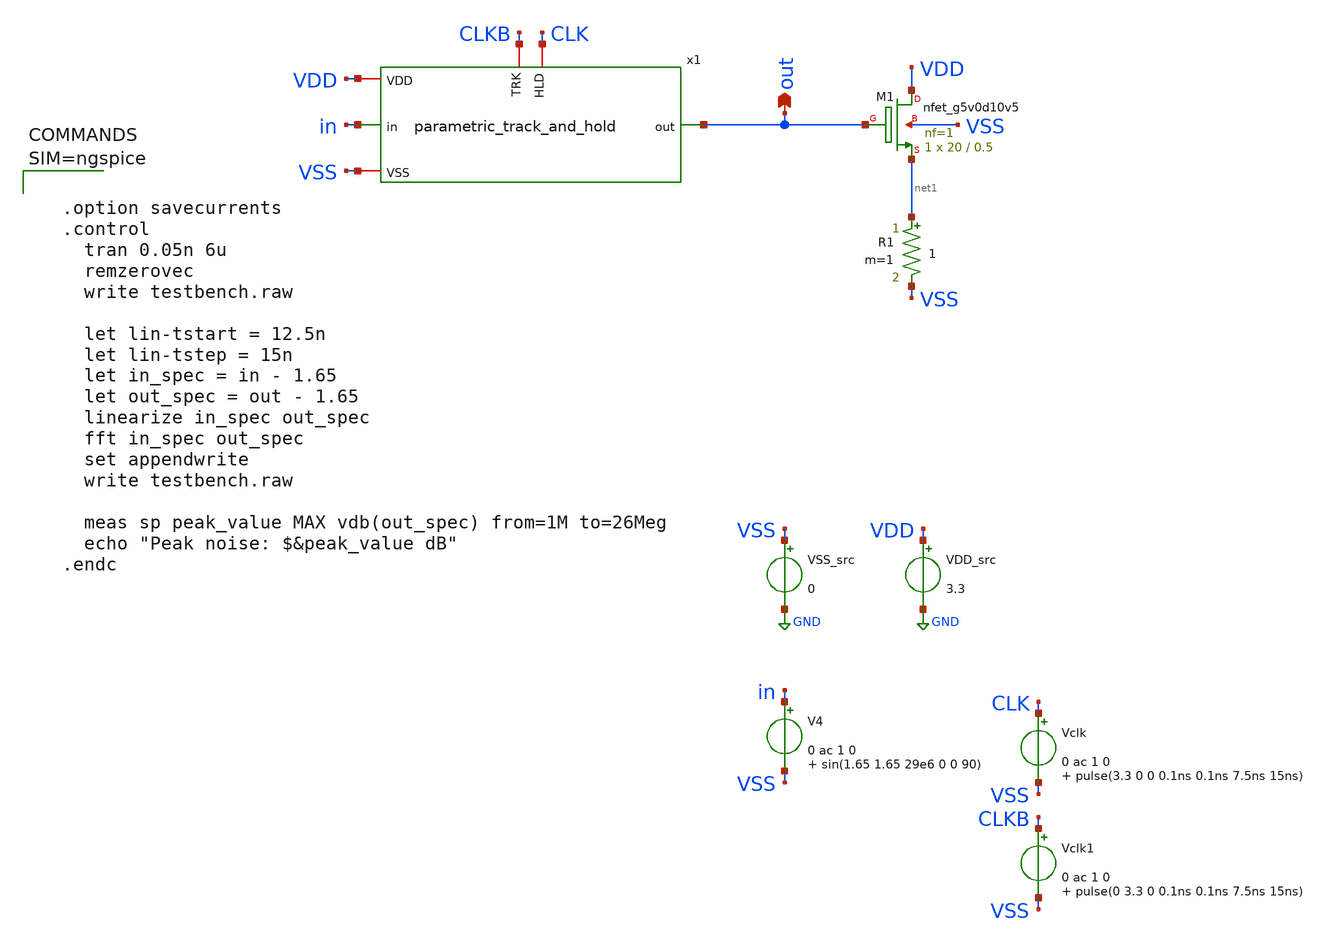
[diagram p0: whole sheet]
** sch_path: xschem/testbench.sch
**.subckt testbench out
*.opin out
VDD_src VDD GND 3.3
VSS_src VSS GND 0
V4 in VSS 0 ac 1 0 sin(1.65 1.65 29e6 0 0 90)
XM1 VDD out net1 VSS sky130_fd_pr__nfet_g5v0d10v5 L=0.5 W=20 nf=1 ad='int((nf+1)/2) * W/nf * 0.29' as='int((nf+2)/2) * W/nf * 0.29'
+ pd='2*int((nf+1)/2) * (W/nf + 0.29)' ps='2*int((nf+2)/2) * (W/nf + 0.29)' nrd='0.29 / W' nrs='0.29 / W'
+ sa=0 sb=0 sd=0 mult=1 m=1
R1 net1 VSS 1 m=1
Vclk CLK VSS 0 ac 1 0 pulse(3.3 0 0 0.1ns 0.1ns 7.5ns 15ns)
Vclk1 CLKB VSS 0 ac 1 0 pulse(0 3.3 0 0.1ns 0.1ns 7.5ns 15ns)
x1 CLK CLKB VDD VSS out in parametric_track_and_hold WT=1 PFT=1.21 PF=2 WS=5 WB=5 CB=18
**** begin user architecture code

** opencircuitdesign pdks install
.lib $::SKYWATER_MODELS/sky130.lib.spice tt





  .option savecurrents
  .control
    tran 0.05n 6u
    remzerovec
    write testbench.raw

    let lin-tstart = 12.5n
    let lin-tstep = 15n
    let in_spec = in - 1.65
    let out_spec = out - 1.65
    linearize in_spec out_spec
    fft in_spec out_spec
    set appendwrite
    write testbench.raw

    meas sp peak_value MAX vdb(out_spec) from=1M to=26Meg
    echo "Peak noise: $&peak_value dB"
  .endc



**** end user architecture code
**.ends

* expanding   symbol:  parametric_track_and_hold.sym # of pins=6
** sym_path: xschem/parametric_track_and_hold.sym
** sch_path: xschem/parametric_track_and_hold.sch
.subckt parametric_track_and_hold HLD TRK VDD VSS out in  WT=1 PFT=1.21 PF=2 WS=5 WB=5 CB=18
*.iopin VSS
*.iopin VDD
*.ipin in
*.opin out
*.iopin TRK
*.iopin HLD
XC1 out VSS sky130_fd_pr__cap_mim_m3_1 W=5 L=5 MF=1 m=1
XM1 out X in VSS sky130_fd_pr__nfet_g5v0d10v5 L=0.5 W={WT} nf=1 ad='int((nf+1)/2) * W/nf * 0.29' as='int((nf+2)/2) * W/nf * 0.29'
+ pd='2*int((nf+1)/2) * (W/nf + 0.29)' ps='2*int((nf+2)/2) * (W/nf + 0.29)' nrd='0.29 / W' nrs='0.29 / W'
+ sa=0 sb=0 sd=0 mult=1 m=1
XM1p out net1 in VDD sky130_fd_pr__pfet_g5v0d10v5 L=0.5 W={WT*PFT} nf=1 ad='int((nf+1)/2) * W/nf * 0.29'
+ as='int((nf+2)/2) * W/nf * 0.29' pd='2*int((nf+1)/2) * (W/nf + 0.29)' ps='2*int((nf+2)/2) * (W/nf + 0.29)'
+ nrd='0.29 / W' nrs='0.29 / W' sa=0 sb=0 sd=0 mult=1 m=1
XM4 VSS HLD X VSS sky130_fd_pr__nfet_g5v0d10v5 L=0.5 W={WS} nf=1 ad='int((nf+1)/2) * W/nf * 0.29' as='int((nf+2)/2) * W/nf * 0.29'
+ pd='2*int((nf+1)/2) * (W/nf + 0.29)' ps='2*int((nf+2)/2) * (W/nf + 0.29)' nrd='0.29 / W' nrs='0.29 / W'
+ sa=0 sb=0 sd=0 mult=1 m=1
XM4p net1 TRK VDD VDD sky130_fd_pr__pfet_g5v0d10v5 L=0.5 W={WS*PF} nf=1 ad='int((nf+1)/2) * W/nf * 0.29'
+ as='int((nf+2)/2) * W/nf * 0.29' pd='2*int((nf+1)/2) * (W/nf + 0.29)' ps='2*int((nf+2)/2) * (W/nf + 0.29)'
+ nrd='0.29 / W' nrs='0.29 / W' sa=0 sb=0 sd=0 mult=1 m=1
XM2 X HLD P P sky130_fd_pr__pfet_g5v0d10v5 L=0.5 W={WS*PF} nf=1 ad='int((nf+1)/2) * W/nf * 0.29' as='int((nf+2)/2) * W/nf * 0.29'
+ pd='2*int((nf+1)/2) * (W/nf + 0.29)' ps='2*int((nf+2)/2) * (W/nf + 0.29)' nrd='0.29 / W' nrs='0.29 / W'
+ sa=0 sb=0 sd=0 mult=1 m=1
XM2p net2 TRK net1 net2 sky130_fd_pr__nfet_g5v0d10v5 L=0.5 W={WS} nf=1 ad='int((nf+1)/2) * W/nf * 0.29'
+ as='int((nf+2)/2) * W/nf * 0.29' pd='2*int((nf+1)/2) * (W/nf + 0.29)' ps='2*int((nf+2)/2) * (W/nf + 0.29)'
+ nrd='0.29 / W' nrs='0.29 / W' sa=0 sb=0 sd=0 mult=1 m=1
XM3 in X Q VSS sky130_fd_pr__nfet_g5v0d10v5 L=0.5 W={WB} nf=1 ad='int((nf+1)/2) * W/nf * 0.29' as='int((nf+2)/2) * W/nf * 0.29'
+ pd='2*int((nf+1)/2) * (W/nf + 0.29)' ps='2*int((nf+2)/2) * (W/nf + 0.29)' nrd='0.29 / W' nrs='0.29 / W'
+ sa=0 sb=0 sd=0 mult=1 m=1
XM6 Q HLD VSS VSS sky130_fd_pr__nfet_g5v0d10v5 L=0.5 W={WB} nf=1 ad='int((nf+1)/2) * W/nf * 0.29' as='int((nf+2)/2) * W/nf * 0.29'
+ pd='2*int((nf+1)/2) * (W/nf + 0.29)' ps='2*int((nf+2)/2) * (W/nf + 0.29)' nrd='0.29 / W' nrs='0.29 / W'
+ sa=0 sb=0 sd=0 mult=1 m=1
XM3p net3 net1 in VDD sky130_fd_pr__pfet_g5v0d10v5 L=0.5 W={WB*PF} nf=1 ad='int((nf+1)/2) * W/nf * 0.29'
+ as='int((nf+2)/2) * W/nf * 0.29' pd='2*int((nf+1)/2) * (W/nf + 0.29)' ps='2*int((nf+2)/2) * (W/nf + 0.29)'
+ nrd='0.29 / W' nrs='0.29 / W' sa=0 sb=0 sd=0 mult=1 m=1
XM6p VDD TRK net3 VDD sky130_fd_pr__pfet_g5v0d10v5 L=0.5 W={WB*PF} nf=1 ad='int((nf+1)/2) * W/nf * 0.29'
+ as='int((nf+2)/2) * W/nf * 0.29' pd='2*int((nf+1)/2) * (W/nf + 0.29)' ps='2*int((nf+2)/2) * (W/nf + 0.29)'
+ nrd='0.29 / W' nrs='0.29 / W' sa=0 sb=0 sd=0 mult=1 m=1
XM5 P X VDD P sky130_fd_pr__pfet_g5v0d10v5 L=0.5 W={WB*PF} nf=1 ad='int((nf+1)/2) * W/nf * 0.29' as='int((nf+2)/2) * W/nf * 0.29'
+ pd='2*int((nf+1)/2) * (W/nf + 0.29)' ps='2*int((nf+2)/2) * (W/nf + 0.29)' nrd='0.29 / W' nrs='0.29 / W'
+ sa=0 sb=0 sd=0 mult=1 m=1
XCb P Q sky130_fd_pr__cap_mim_m3_1 W={CB} L={CB} MF=1 m=1
XCbp net2 net3 sky130_fd_pr__cap_mim_m3_1 W={CB} L={CB} MF=1 m=1
XM5p VSS net1 net2 net2 sky130_fd_pr__nfet_g5v0d10v5 L=0.5 W={WB*PF} nf=1 ad='int((nf+1)/2) * W/nf * 0.29'
+ as='int((nf+2)/2) * W/nf * 0.29' pd='2*int((nf+1)/2) * (W/nf + 0.29)' ps='2*int((nf+2)/2) * (W/nf + 0.29)'
+ nrd='0.29 / W' nrs='0.29 / W' sa=0 sb=0 sd=0 mult=1 m=1
.ends

.GLOBAL GND
.end
